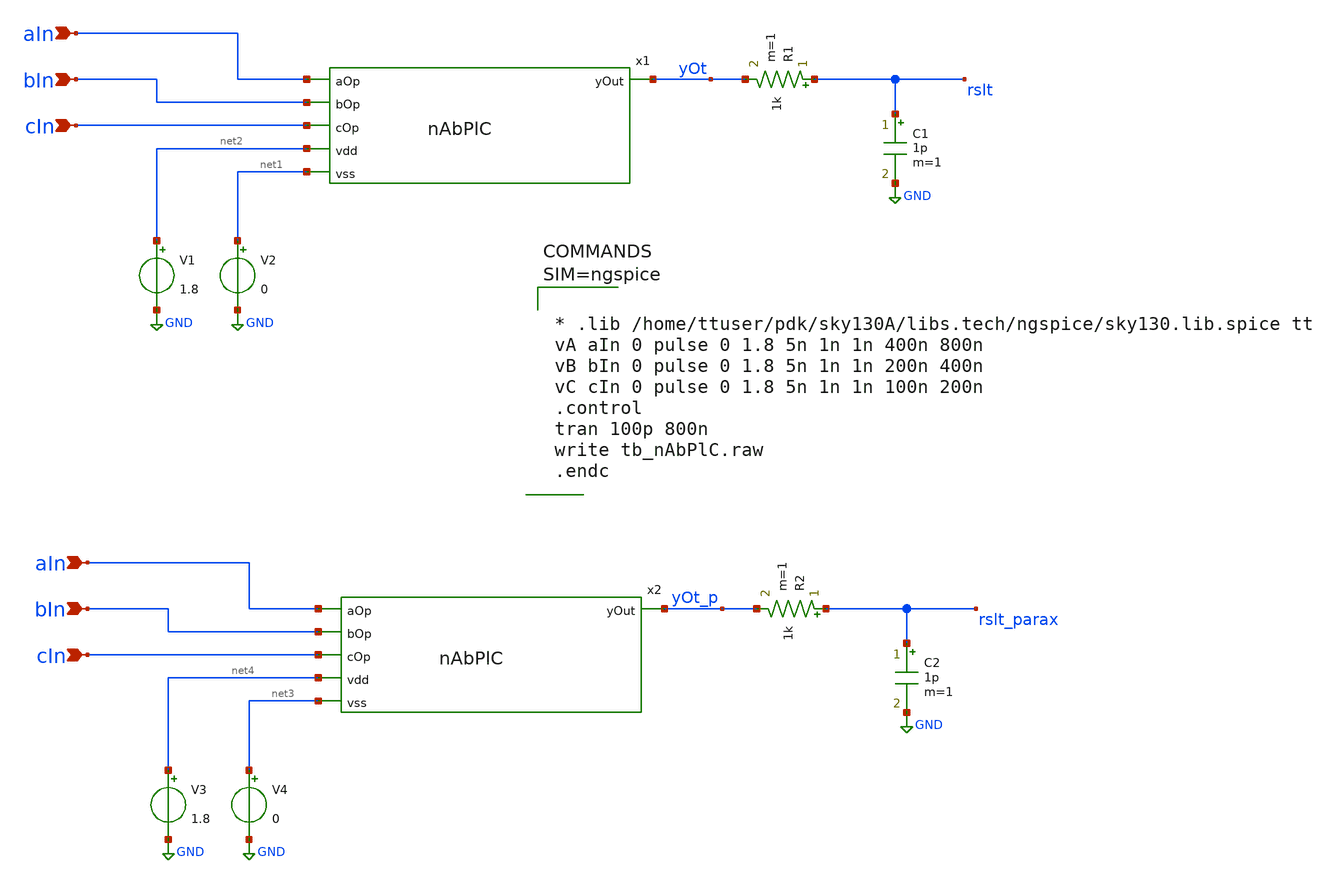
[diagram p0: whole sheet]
** sch_path: xschem/tb_nAbPlC.sch
**.subckt tb_nAbPlC bIn aIn cIn bIn aIn cIn
*.ipin bIn
*.ipin aIn
*.ipin cIn
*.ipin bIn
*.ipin aIn
*.ipin cIn
R1 rslt yOt 1k m=1
C1 rslt GND 1p m=1
V1 net2 GND 1.8
V2 net1 GND 0
x1 aIn bIn cIn net2 yOt net1 nAbPlC
R2 rslt_parax yOt_p 1k m=1
C2 rslt_parax GND 1p m=1
V3 net4 GND 1.8
V4 net3 GND 0
x2 aIn bIn cIn net4 yOt_p net3 nAbPlC_parax
**** begin user architecture code

** opencircuitdesign pdks install
.lib $::SKYWATER_MODELS/sky130.lib.spice tt





* .lib /home/ttuser/pdk/sky130A/libs.tech/ngspice/sky130.lib.spice tt
vA aIn 0 pulse 0 1.8 5n 1n 1n 400n 800n
vB bIn 0 pulse 0 1.8 5n 1n 1n 200n 400n
vC cIn 0 pulse 0 1.8 5n 1n 1n 100n 200n
.control
tran 100p 800n
write tb_nAbPlC.raw
.endc



**** end user architecture code
**.ends

* expanding   symbol:  nAbPlC.sym # of pins=6
** sym_path: xschem/nAbPlC.sym
** sch_path: xschem/nAbPlC.sch
.subckt nAbPlC aOp bOp cOp vdd yOut vss
*.ipin aOp
*.ipin bOp
*.ipin cOp
*.ipin vdd
*.ipin vss
*.opin yOut
XM1 ab_c aOp vdd vdd sky130_fd_pr__pfet_01v8 L=0.15 W=1 nf=1 ad='int((nf+1)/2) * W/nf * 0.29' as='int((nf+2)/2) * W/nf * 0.29'
+ pd='2*int((nf+1)/2) * (W/nf + 0.29)' ps='2*int((nf+2)/2) * (W/nf + 0.29)' nrd='0.29 / W' nrs='0.29 / W'
+ sa=0 sb=0 sd=0 mult=1 m=1
XM2 ab_c bOp vdd vdd sky130_fd_pr__pfet_01v8 L=0.15 W=1 nf=1 ad='int((nf+1)/2) * W/nf * 0.29' as='int((nf+2)/2) * W/nf * 0.29'
+ pd='2*int((nf+1)/2) * (W/nf + 0.29)' ps='2*int((nf+2)/2) * (W/nf + 0.29)' nrd='0.29 / W' nrs='0.29 / W'
+ sa=0 sb=0 sd=0 mult=1 m=1
XM3 yOut cOp ab_c vdd sky130_fd_pr__pfet_01v8 L=0.15 W=1 nf=1 ad='int((nf+1)/2) * W/nf * 0.29' as='int((nf+2)/2) * W/nf * 0.29'
+ pd='2*int((nf+1)/2) * (W/nf + 0.29)' ps='2*int((nf+2)/2) * (W/nf + 0.29)' nrd='0.29 / W' nrs='0.29 / W'
+ sa=0 sb=0 sd=0 mult=1 m=1
XM4 yOut aOp a_b vss sky130_fd_pr__nfet_01v8 L=0.15 W=1 nf=1 ad='int((nf+1)/2) * W/nf * 0.29' as='int((nf+2)/2) * W/nf * 0.29'
+ pd='2*int((nf+1)/2) * (W/nf + 0.29)' ps='2*int((nf+2)/2) * (W/nf + 0.29)' nrd='0.29 / W' nrs='0.29 / W'
+ sa=0 sb=0 sd=0 mult=1 m=1
XM5 a_b bOp vss vss sky130_fd_pr__nfet_01v8 L=0.15 W=1 nf=1 ad='int((nf+1)/2) * W/nf * 0.29' as='int((nf+2)/2) * W/nf * 0.29'
+ pd='2*int((nf+1)/2) * (W/nf + 0.29)' ps='2*int((nf+2)/2) * (W/nf + 0.29)' nrd='0.29 / W' nrs='0.29 / W'
+ sa=0 sb=0 sd=0 mult=1 m=1
XM6 yOut cOp vss vss sky130_fd_pr__nfet_01v8 L=0.15 W=1 nf=1 ad='int((nf+1)/2) * W/nf * 0.29' as='int((nf+2)/2) * W/nf * 0.29'
+ pd='2*int((nf+1)/2) * (W/nf + 0.29)' ps='2*int((nf+2)/2) * (W/nf + 0.29)' nrd='0.29 / W' nrs='0.29 / W'
+ sa=0 sb=0 sd=0 mult=1 m=1
.ends


* expanding   symbol:  nAbPlC_parax.sym # of pins=6
** sym_path: xschem/nAbPlC.sym
.include [file normalize ../mag/nAbPlC.sim.spice]
.GLOBAL GND
.end
